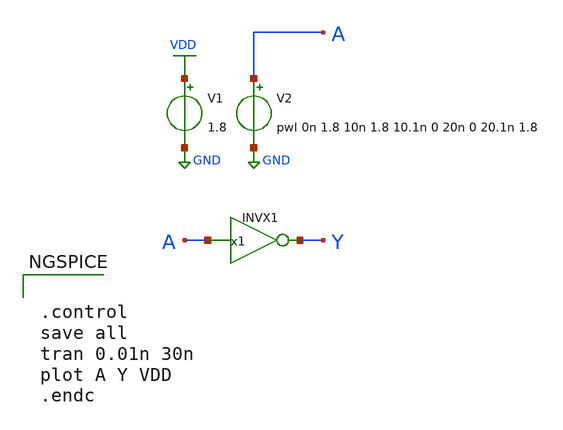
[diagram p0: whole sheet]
** sch_path: lib/xschem/test_INVX1.sch
**.subckt test_INVX1
V2 A GND pwl 0n 1.8 10n 1.8 10.1n 0 20n 0 20.1n 1.8
V1 VDD GND 1.8
x1 Y A VDD GND INVX1
**** begin user architecture code

.lib $::SKYWATER_MODELS/sky130.lib.spice tt


**** end user architecture code
**.ends

* expanding   symbol:  INVX1.sym # of pins=2
** sym_path: lib/xschem/INVX1.sym
** sch_path: lib/xschem/INVX1.sch
.subckt INVX1 Y A VCCPIN VSSPIN
*.ipin A
*.opin Y
XM1 Y A VSSPIN VSSPIN sky130_fd_pr__nfet_01v8 L=0.15 W=3 nf=1 ad='int((nf+1)/2) * W/nf * 0.29' as='int((nf+2)/2) * W/nf * 0.29'
+ pd='2*int((nf+1)/2) * (W/nf + 0.29)' ps='2*int((nf+2)/2) * (W/nf + 0.29)' nrd='0.29 / W' nrs='0.29 / W'
+ sa=0 sb=0 sd=0 mult=1 m=1
XM2 Y A VCCPIN VCCPIN sky130_fd_pr__pfet_01v8 L=0.15 W=2 nf=1 ad='int((nf+1)/2) * W/nf * 0.29' as='int((nf+2)/2) * W/nf * 0.29'
+ pd='2*int((nf+1)/2) * (W/nf + 0.29)' ps='2*int((nf+2)/2) * (W/nf + 0.29)' nrd='0.29 / W' nrs='0.29 / W'
+ sa=0 sb=0 sd=0 mult=1 m=1
XM3 Y A VCCPIN VCCPIN sky130_fd_pr__pfet_01v8 L=0.15 W=2 nf=1 ad='int((nf+1)/2) * W/nf * 0.29' as='int((nf+2)/2) * W/nf * 0.29'
+ pd='2*int((nf+1)/2) * (W/nf + 0.29)' ps='2*int((nf+2)/2) * (W/nf + 0.29)' nrd='0.29 / W' nrs='0.29 / W'
+ sa=0 sb=0 sd=0 mult=1 m=1
.ends

.GLOBAL VDD
.GLOBAL GND
**** begin user architecture code


.control
save all
tran 0.01n 30n
plot A Y VDD
.endc


**** end user architecture code
.end
